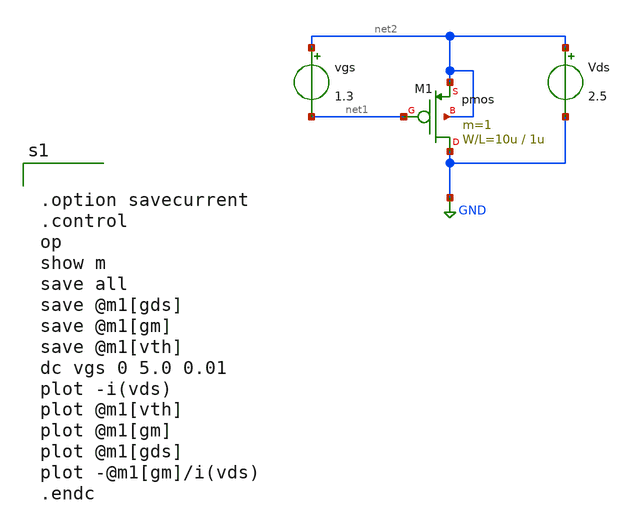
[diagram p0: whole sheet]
** sch_path: member_project/GroupWork/Team_masahiro/pfet_id-vgs.sch
**.subckt pfet_id-vgs
M1 GND net1 net2 net2 pmos L=1u W=10u m=1
vgs net2 net1 1.3
Vds net2 GND 2.5
**** begin user architecture code
 .include $::LIB/mos.lib
.include $::LIB/passive.lib
.include $::LIB/diode.lib


.option savecurrent
.control
op
show m
save all
save @m1[gds]
save @m1[gm]
save @m1[vth]
dc vgs 0 5.0 0.01
plot -i(vds)
plot @m1[vth]
plot @m1[gm]
plot @m1[gds]
plot -@m1[gm]/i(vds)
.endc


**** end user architecture code
**.ends
.GLOBAL GND
.end
